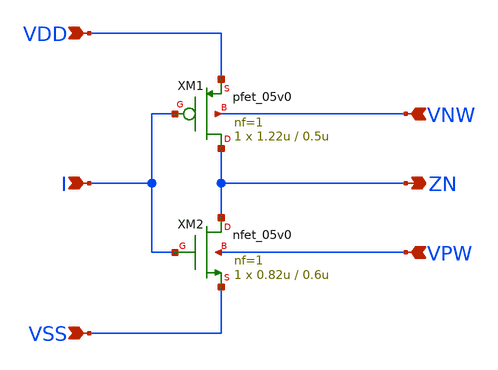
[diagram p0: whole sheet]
** sch_path: flows/smoke/inverter/inverter.sch
* SPDX-License-Identifier: Apache-2.0
**.subckt inverter I ZN VDD VNW VPW VSS
*.ipin I
*.opin ZN
*.ipin VDD
*.ipin VNW
*.ipin VPW
*.ipin VSS
XM1 ZN I VDD VNW pfet_05v0 L=0.5u W=1.22u nf=1 ad='int((nf+1)/2) * W/nf * 0.3u' as='int((nf+2)/2) * W/nf * 0.3u'
+ pd='2*int((nf+1)/2) * (W/nf + 0.3u)' ps='2*int((nf+2)/2) * (W/nf + 0.3u)' nrd='0.3u / W' nrs='0.3u / W'
+ sa=0 sb=0 sd=0 m=1
XM2 ZN I VSS VPW nfet_05v0 L=0.6u W=0.82u nf=1 ad='int((nf+1)/2) * W/nf * 0.3u' as='int((nf+2)/2) * W/nf * 0.3u'
+ pd='2*int((nf+1)/2) * (W/nf + 0.3u)' ps='2*int((nf+2)/2) * (W/nf + 0.3u)' nrd='0.3u / W' nrs='0.3u / W'
+ sa=0 sb=0 sd=0 m=1
**.ends
.end
